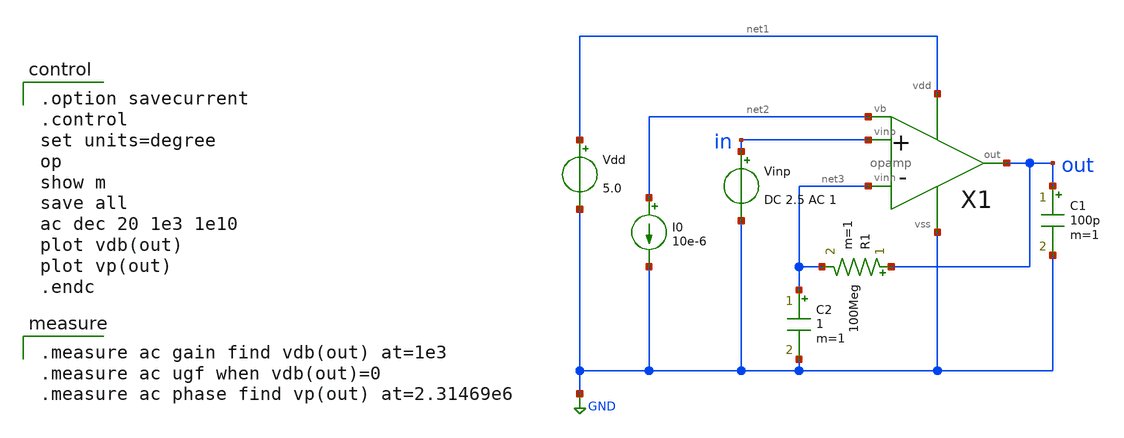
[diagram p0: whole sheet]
** sch_path: member_project/opamp/houta/opamp_ac_other.sch
**.subckt opamp_ac_other
Vdd net1 GND 5.0
Vinp in GND DC 2.5 AC 1
C1 out GND 100p m=1
X1 in net3 net2 out net1 GND opamp
I0 net2 GND 10e-6
R1 out net3 100Meg m=1
C2 net3 GND 1 m=1
**** begin user architecture code

.option savecurrent
.control
set units=degree
op
show m
save all
ac dec 20 1e3 1e10
plot vdb(out)
plot vp(out)
.endc


.measure ac gain find vdb(out) at=1e3
.measure ac ugf when vdb(out)=0
.measure ac phase find vp(out) at=2.31469e6

 .include $::LIB/ip62_models
**** end user architecture code
**.ends

* expanding   symbol:  opamp.sym # of pins=6
** sym_path: member_project/LPF/noritsuna/xschem/opamp.sym
** sch_path: member_project/LPF/noritsuna/xschem/opamp.sch
.subckt opamp vinp vinn vb out vdd vss
*.ipin vinp
*.ipin vinn
*.opin out
*.iopin vdd
*.iopin vss
*.iopin vb
X1 vinp vinn net2 vdd vss net5 diff
X2 net2 net5 out vdd vss cs
XM9 net1 net5 vdd vdd PMOS w=30u l=1u as=0 ad=0 ps=0 pd=0 nrd=0 nrs=0 m=1
XM12 net3 net1 net2 vss NMOS w=20u l=1u as=0 ad=0 ps=0 pd=0 nrd=0 nrs=0 m=1
XM1 net5 net5 vdd vdd PMOS w=30u l=1u as=0 ad=0 ps=0 pd=0 nrd=0 nrs=0 m=1
XM10 net1 net1 net4 vss NMOS w=10u l=1u as=0 ad=0 ps=0 pd=0 nrd=0 nrs=0 m=1
XM11 net4 net4 vss vss NMOS w=10u l=1u as=0 ad=0 ps=0 pd=0 nrd=0 nrs=0 m=1
XC1 net3 out vss F_CSIO c=8.856p x=120u y=120u m=1
XM2 net5 vb vss vss NMOS w=10u l=1u as=0 ad=0 ps=0 pd=0 nrd=0 nrs=0 m=1
.ends


* expanding   symbol:  diff.sym # of pins=6
** sym_path: diff.sym
** sch_path: diff.sch
.subckt diff vinp vinn out vdd vss vb
*.ipin vinn
*.ipin vinp
*.ipin vb
*.opin out
*.iopin vdd
*.iopin vss
XM5 net2 vb vdd vdd PMOS w=220u l=2u as=0 ad=0 ps=0 pd=0 nrd=0 nrs=0 m=1
XM1 net1 vinn net2 net2 PMOS w=500u l=2u as=0 ad=0 ps=0 pd=0 nrd=0 nrs=0 m=1
XM2 out vinp net2 net2 PMOS w=500u l=2u as=0 ad=0 ps=0 pd=0 nrd=0 nrs=0 m=1
XM3 net1 net1 vss vss NMOS w=40u l=2u as=0 ad=0 ps=0 pd=0 nrd=0 nrs=0 m=1
XM4 out net1 vss vss NMOS w=40u l=2u as=0 ad=0 ps=0 pd=0 nrd=0 nrs=0 m=1
.ends


* expanding   symbol:  cs.sym # of pins=5
** sym_path: cs.sym
** sch_path: cs.sch
.subckt cs vin vb out vdd vss
*.ipin vb
*.ipin vin
*.opin out
*.iopin vss
*.iopin vdd
XM6 out vb vdd vdd PMOS w=280u l=2u as=0 ad=0 ps=0 pd=0 nrd=0 nrs=0 m=1
XM7 out vin vss vss NMOS w=100u l=2u as=0 ad=0 ps=0 pd=0 nrd=0 nrs=0 m=1
.ends

.GLOBAL GND
.end
